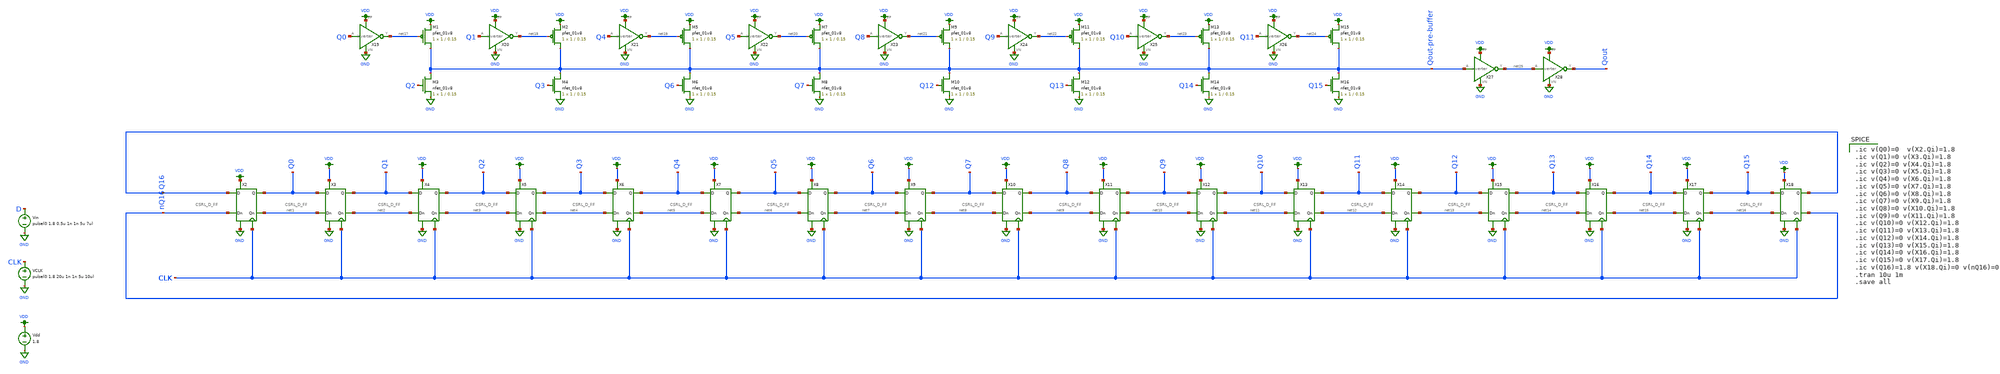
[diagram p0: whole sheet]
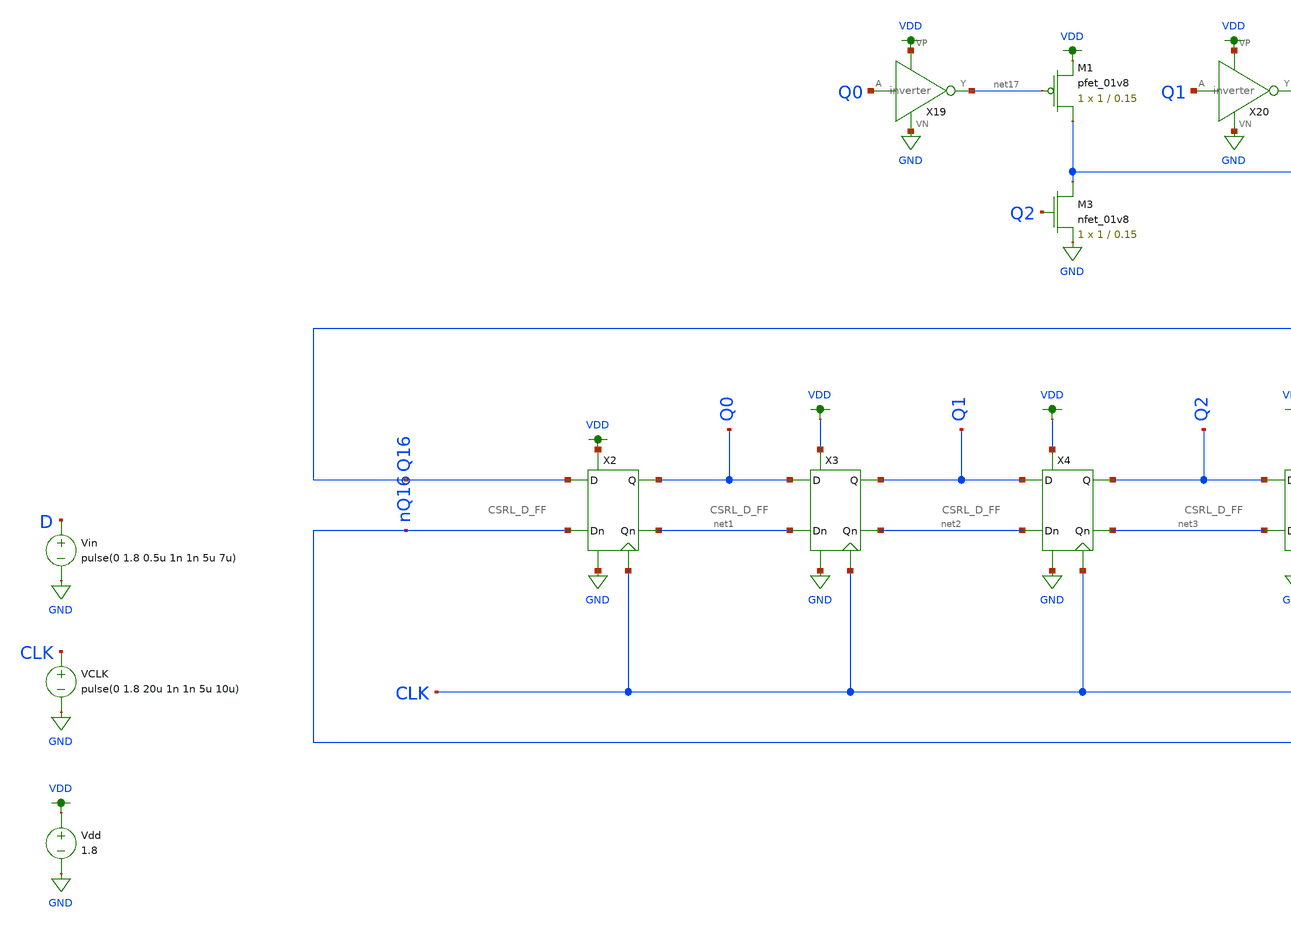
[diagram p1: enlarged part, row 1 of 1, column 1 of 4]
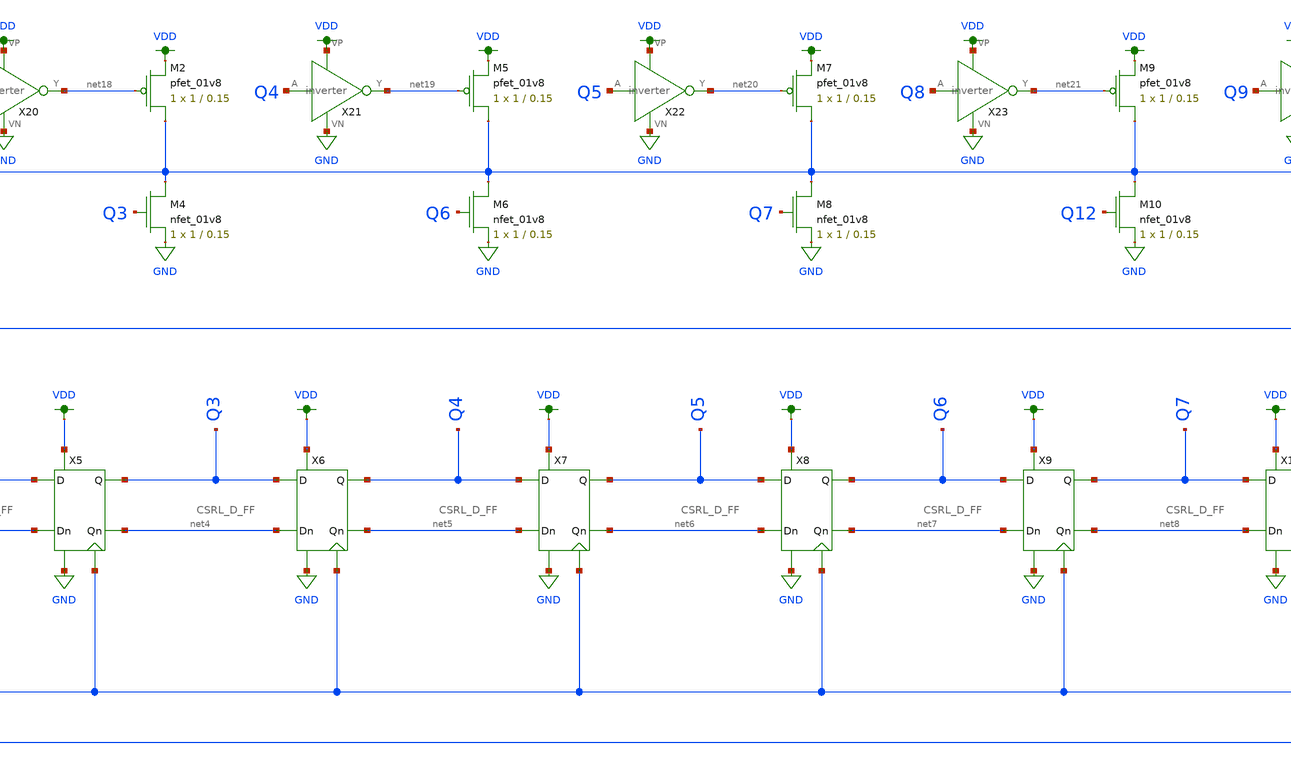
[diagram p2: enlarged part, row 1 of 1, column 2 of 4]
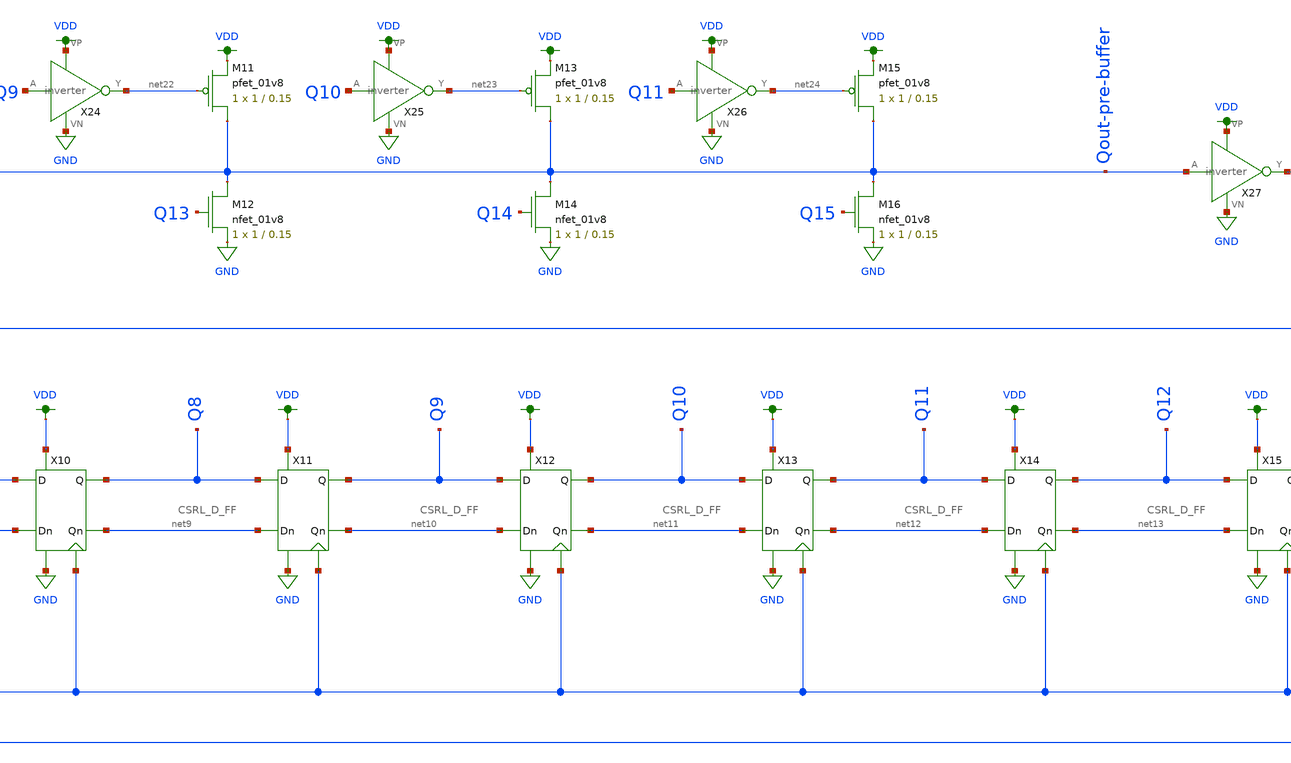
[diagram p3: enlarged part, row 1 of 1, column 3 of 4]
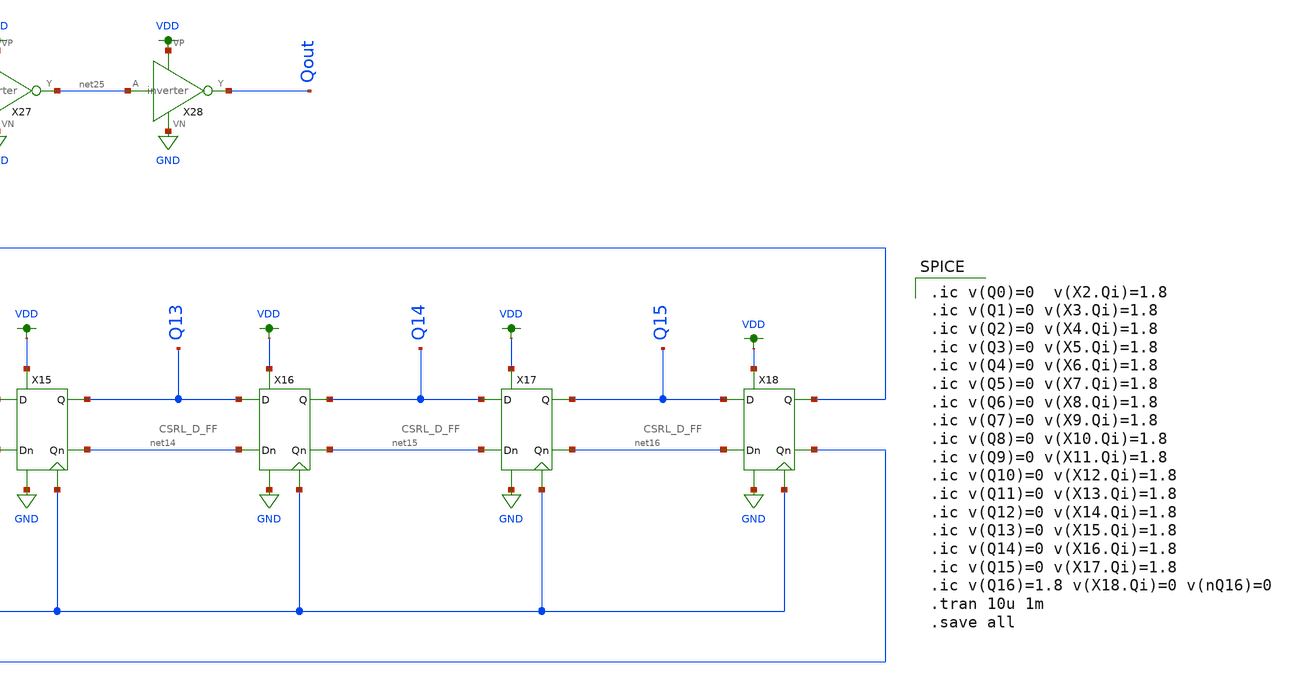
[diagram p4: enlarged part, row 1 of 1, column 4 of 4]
** sch_path: schematic/archive/phi1.sch
**.subckt phi1
Vin D GND pulse(0 1.8 0.5u 1n 1n 5u 7u)
VCLK CLK GND pulse(0 1.8 20u 1n 1n 5u 10u)
Vdd VDD GND 1.8
X2 nQ16 Q16 net1 Q0 GND VDD CLK CSRL_D_FF
X3 net1 Q0 net2 Q1 GND VDD CLK CSRL_D_FF
X4 net2 Q1 net3 Q2 GND VDD CLK CSRL_D_FF
X5 net3 Q2 net4 Q3 GND VDD CLK CSRL_D_FF
X6 net4 Q3 net5 Q4 GND VDD CLK CSRL_D_FF
X7 net5 Q4 net6 Q5 GND VDD CLK CSRL_D_FF
X8 net6 Q5 net7 Q6 GND VDD CLK CSRL_D_FF
X9 net7 Q6 net8 Q7 GND VDD CLK CSRL_D_FF
X10 net8 Q7 net9 Q8 GND VDD CLK CSRL_D_FF
X11 net9 Q8 net10 Q9 GND VDD CLK CSRL_D_FF
X12 net10 Q9 net11 Q10 GND VDD CLK CSRL_D_FF
X13 net11 Q10 net12 Q11 GND VDD CLK CSRL_D_FF
X14 net12 Q11 net13 Q12 GND VDD CLK CSRL_D_FF
X15 net13 Q12 net14 Q13 GND VDD CLK CSRL_D_FF
X16 net14 Q13 net15 Q14 GND VDD CLK CSRL_D_FF
X18 net16 Q15 nQ16 Q16 GND VDD CLK CSRL_D_FF
X17 net15 Q14 net16 Q15 GND VDD CLK CSRL_D_FF
XM1 Qout-pre-buffer net17 VDD VDD sky130_fd_pr__pfet_01v8 L=0.15 W=1 nf=1 ad='int((nf+1)/2) * W/nf * 0.29'
+ as='int((nf+2)/2) * W/nf * 0.29' pd='2*int((nf+1)/2) * (W/nf + 0.29)' ps='2*int((nf+2)/2) * (W/nf + 0.29)'
+ nrd='0.29 / W' nrs='0.29 / W' sa=0 sb=0 sd=0 mult=1 m=1
XM2 Qout-pre-buffer net18 VDD VDD sky130_fd_pr__pfet_01v8 L=0.15 W=1 nf=1 ad='int((nf+1)/2) * W/nf * 0.29'
+ as='int((nf+2)/2) * W/nf * 0.29' pd='2*int((nf+1)/2) * (W/nf + 0.29)' ps='2*int((nf+2)/2) * (W/nf + 0.29)'
+ nrd='0.29 / W' nrs='0.29 / W' sa=0 sb=0 sd=0 mult=1 m=1
X19 Q0 net17 VDD GND inverter
X20 Q1 net18 VDD GND inverter
XM3 Qout-pre-buffer Q2 GND GND sky130_fd_pr__nfet_01v8 L=0.15 W=1 nf=1 ad='int((nf+1)/2) * W/nf * 0.29'
+ as='int((nf+2)/2) * W/nf * 0.29' pd='2*int((nf+1)/2) * (W/nf + 0.29)' ps='2*int((nf+2)/2) * (W/nf + 0.29)'
+ nrd='0.29 / W' nrs='0.29 / W' sa=0 sb=0 sd=0 mult=1 m=1
XM4 Qout-pre-buffer Q3 GND GND sky130_fd_pr__nfet_01v8 L=0.15 W=1 nf=1 ad='int((nf+1)/2) * W/nf * 0.29'
+ as='int((nf+2)/2) * W/nf * 0.29' pd='2*int((nf+1)/2) * (W/nf + 0.29)' ps='2*int((nf+2)/2) * (W/nf + 0.29)'
+ nrd='0.29 / W' nrs='0.29 / W' sa=0 sb=0 sd=0 mult=1 m=1
XM5 Qout-pre-buffer net19 VDD VDD sky130_fd_pr__pfet_01v8 L=0.15 W=1 nf=1 ad='int((nf+1)/2) * W/nf * 0.29'
+ as='int((nf+2)/2) * W/nf * 0.29' pd='2*int((nf+1)/2) * (W/nf + 0.29)' ps='2*int((nf+2)/2) * (W/nf + 0.29)'
+ nrd='0.29 / W' nrs='0.29 / W' sa=0 sb=0 sd=0 mult=1 m=1
X21 Q4 net19 VDD GND inverter
XM6 Qout-pre-buffer Q6 GND GND sky130_fd_pr__nfet_01v8 L=0.15 W=1 nf=1 ad='int((nf+1)/2) * W/nf * 0.29'
+ as='int((nf+2)/2) * W/nf * 0.29' pd='2*int((nf+1)/2) * (W/nf + 0.29)' ps='2*int((nf+2)/2) * (W/nf + 0.29)'
+ nrd='0.29 / W' nrs='0.29 / W' sa=0 sb=0 sd=0 mult=1 m=1
XM7 Qout-pre-buffer net20 VDD VDD sky130_fd_pr__pfet_01v8 L=0.15 W=1 nf=1 ad='int((nf+1)/2) * W/nf * 0.29'
+ as='int((nf+2)/2) * W/nf * 0.29' pd='2*int((nf+1)/2) * (W/nf + 0.29)' ps='2*int((nf+2)/2) * (W/nf + 0.29)'
+ nrd='0.29 / W' nrs='0.29 / W' sa=0 sb=0 sd=0 mult=1 m=1
X22 Q5 net20 VDD GND inverter
XM8 Qout-pre-buffer Q7 GND GND sky130_fd_pr__nfet_01v8 L=0.15 W=1 nf=1 ad='int((nf+1)/2) * W/nf * 0.29'
+ as='int((nf+2)/2) * W/nf * 0.29' pd='2*int((nf+1)/2) * (W/nf + 0.29)' ps='2*int((nf+2)/2) * (W/nf + 0.29)'
+ nrd='0.29 / W' nrs='0.29 / W' sa=0 sb=0 sd=0 mult=1 m=1
XM9 Qout-pre-buffer net21 VDD VDD sky130_fd_pr__pfet_01v8 L=0.15 W=1 nf=1 ad='int((nf+1)/2) * W/nf * 0.29'
+ as='int((nf+2)/2) * W/nf * 0.29' pd='2*int((nf+1)/2) * (W/nf + 0.29)' ps='2*int((nf+2)/2) * (W/nf + 0.29)'
+ nrd='0.29 / W' nrs='0.29 / W' sa=0 sb=0 sd=0 mult=1 m=1
X23 Q8 net21 VDD GND inverter
XM10 Qout-pre-buffer Q12 GND GND sky130_fd_pr__nfet_01v8 L=0.15 W=1 nf=1 ad='int((nf+1)/2) * W/nf * 0.29'
+ as='int((nf+2)/2) * W/nf * 0.29' pd='2*int((nf+1)/2) * (W/nf + 0.29)' ps='2*int((nf+2)/2) * (W/nf + 0.29)'
+ nrd='0.29 / W' nrs='0.29 / W' sa=0 sb=0 sd=0 mult=1 m=1
XM11 Qout-pre-buffer net22 VDD VDD sky130_fd_pr__pfet_01v8 L=0.15 W=1 nf=1 ad='int((nf+1)/2) * W/nf * 0.29'
+ as='int((nf+2)/2) * W/nf * 0.29' pd='2*int((nf+1)/2) * (W/nf + 0.29)' ps='2*int((nf+2)/2) * (W/nf + 0.29)'
+ nrd='0.29 / W' nrs='0.29 / W' sa=0 sb=0 sd=0 mult=1 m=1
X24 Q9 net22 VDD GND inverter
XM12 Qout-pre-buffer Q13 GND GND sky130_fd_pr__nfet_01v8 L=0.15 W=1 nf=1 ad='int((nf+1)/2) * W/nf * 0.29'
+ as='int((nf+2)/2) * W/nf * 0.29' pd='2*int((nf+1)/2) * (W/nf + 0.29)' ps='2*int((nf+2)/2) * (W/nf + 0.29)'
+ nrd='0.29 / W' nrs='0.29 / W' sa=0 sb=0 sd=0 mult=1 m=1
XM13 Qout-pre-buffer net23 VDD VDD sky130_fd_pr__pfet_01v8 L=0.15 W=1 nf=1 ad='int((nf+1)/2) * W/nf * 0.29'
+ as='int((nf+2)/2) * W/nf * 0.29' pd='2*int((nf+1)/2) * (W/nf + 0.29)' ps='2*int((nf+2)/2) * (W/nf + 0.29)'
+ nrd='0.29 / W' nrs='0.29 / W' sa=0 sb=0 sd=0 mult=1 m=1
X25 Q10 net23 VDD GND inverter
XM14 Qout-pre-buffer Q14 GND GND sky130_fd_pr__nfet_01v8 L=0.15 W=1 nf=1 ad='int((nf+1)/2) * W/nf * 0.29'
+ as='int((nf+2)/2) * W/nf * 0.29' pd='2*int((nf+1)/2) * (W/nf + 0.29)' ps='2*int((nf+2)/2) * (W/nf + 0.29)'
+ nrd='0.29 / W' nrs='0.29 / W' sa=0 sb=0 sd=0 mult=1 m=1
XM15 Qout-pre-buffer net24 VDD VDD sky130_fd_pr__pfet_01v8 L=0.15 W=1 nf=1 ad='int((nf+1)/2) * W/nf * 0.29'
+ as='int((nf+2)/2) * W/nf * 0.29' pd='2*int((nf+1)/2) * (W/nf + 0.29)' ps='2*int((nf+2)/2) * (W/nf + 0.29)'
+ nrd='0.29 / W' nrs='0.29 / W' sa=0 sb=0 sd=0 mult=1 m=1
X26 Q11 net24 VDD GND inverter
XM16 Qout-pre-buffer Q15 GND GND sky130_fd_pr__nfet_01v8 L=0.15 W=1 nf=1 ad='int((nf+1)/2) * W/nf * 0.29'
+ as='int((nf+2)/2) * W/nf * 0.29' pd='2*int((nf+1)/2) * (W/nf + 0.29)' ps='2*int((nf+2)/2) * (W/nf + 0.29)'
+ nrd='0.29 / W' nrs='0.29 / W' sa=0 sb=0 sd=0 mult=1 m=1
X27 Qout-pre-buffer net25 VDD GND inverter
X28 net25 Qout VDD GND inverter
**** begin user architecture code

.ic v(Q0)=0  v(X2.Qi)=1.8
.ic v(Q1)=0 v(X3.Qi)=1.8
.ic v(Q2)=0 v(X4.Qi)=1.8
.ic v(Q3)=0 v(X5.Qi)=1.8
.ic v(Q4)=0 v(X6.Qi)=1.8
.ic v(Q5)=0 v(X7.Qi)=1.8
.ic v(Q6)=0 v(X8.Qi)=1.8
.ic v(Q7)=0 v(X9.Qi)=1.8
.ic v(Q8)=0 v(X10.Qi)=1.8
.ic v(Q9)=0 v(X11.Qi)=1.8
.ic v(Q10)=0 v(X12.Qi)=1.8
.ic v(Q11)=0 v(X13.Qi)=1.8
.ic v(Q12)=0 v(X14.Qi)=1.8
.ic v(Q13)=0 v(X15.Qi)=1.8
.ic v(Q14)=0 v(X16.Qi)=1.8
.ic v(Q15)=0 v(X17.Qi)=1.8
.ic v(Q16)=1.8 v(X18.Qi)=0 v(nQ16)=0
.tran 10u 1m
.save all


.option wnflag=1
.param MC_SWITCH=0.0
.lib /media/qdeng/526448C32060CF5C/skywater/skywater-pdk/libraries/sky130_fd_pr_ngspice/latest/models/sky130.lib.spice tt

**** end user architecture code
**.ends

* expanding   symbol:  /home/madvlsi/Documents/MADVLSI-Final_Project/schematic/CSRL_D_FF.sym # of
*+ pins=7
** sym_path: schematic/CSRL_D_FF.sym
** sch_path: schematic/CSRL_D_FF.sch
.subckt CSRL_D_FF Dn D Qn Q VN VP CLK
*.ipin Dn
*.ipin D
*.iopin VP
*.iopin VN
*.iopin CLK
*.opin Qn
*.opin Q
XM1 net5 CLK VP VDD sky130_fd_pr__pfet_01v8 L=0.15 W=1 nf=1 ad='int((nf+1)/2) * W/nf * 0.29' as='int((nf+2)/2) * W/nf * 0.29'
+ pd='2*int((nf+1)/2) * (W/nf + 0.29)' ps='2*int((nf+2)/2) * (W/nf + 0.29)' nrd='0.29 / W' nrs='0.29 / W'
+ sa=0 sb=0 sd=0 mult=1 m=1
XM2 net6 CLK VP VDD sky130_fd_pr__pfet_01v8 L=0.15 W=1 nf=1 ad='int((nf+1)/2) * W/nf * 0.29' as='int((nf+2)/2) * W/nf * 0.29'
+ pd='2*int((nf+1)/2) * (W/nf + 0.29)' ps='2*int((nf+2)/2) * (W/nf + 0.29)' nrd='0.29 / W' nrs='0.29 / W'
+ sa=0 sb=0 sd=0 mult=1 m=1
XM3 net3 CLK Q GND sky130_fd_pr__nfet_01v8 L=0.15 W=1 nf=1 ad='int((nf+1)/2) * W/nf * 0.29' as='int((nf+2)/2) * W/nf * 0.29'
+ pd='2*int((nf+1)/2) * (W/nf + 0.29)' ps='2*int((nf+2)/2) * (W/nf + 0.29)' nrd='0.29 / W' nrs='0.29 / W'
+ sa=0 sb=0 sd=0 mult=1 m=1
XM4 net4 CLK Qn GND sky130_fd_pr__nfet_01v8 L=0.15 W=1 nf=1 ad='int((nf+1)/2) * W/nf * 0.29' as='int((nf+2)/2) * W/nf * 0.29'
+ pd='2*int((nf+1)/2) * (W/nf + 0.29)' ps='2*int((nf+2)/2) * (W/nf + 0.29)' nrd='0.29 / W' nrs='0.29 / W'
+ sa=0 sb=0 sd=0 mult=1 m=1
XM5 Q Qn net6 VDD sky130_fd_pr__pfet_01v8 L=0.15 W=1 nf=1 ad='int((nf+1)/2) * W/nf * 0.29' as='int((nf+2)/2) * W/nf * 0.29'
+ pd='2*int((nf+1)/2) * (W/nf + 0.29)' ps='2*int((nf+2)/2) * (W/nf + 0.29)' nrd='0.29 / W' nrs='0.29 / W'
+ sa=0 sb=0 sd=0 mult=1 m=1
XM6 VN Qn Q GND sky130_fd_pr__nfet_01v8 L=0.15 W=1 nf=1 ad='int((nf+1)/2) * W/nf * 0.29' as='int((nf+2)/2) * W/nf * 0.29'
+ pd='2*int((nf+1)/2) * (W/nf + 0.29)' ps='2*int((nf+2)/2) * (W/nf + 0.29)' nrd='0.29 / W' nrs='0.29 / W'
+ sa=0 sb=0 sd=0 mult=1 m=1
XM7 Qn Q net5 VDD sky130_fd_pr__pfet_01v8 L=0.15 W=1 nf=1 ad='int((nf+1)/2) * W/nf * 0.29' as='int((nf+2)/2) * W/nf * 0.29'
+ pd='2*int((nf+1)/2) * (W/nf + 0.29)' ps='2*int((nf+2)/2) * (W/nf + 0.29)' nrd='0.29 / W' nrs='0.29 / W'
+ sa=0 sb=0 sd=0 mult=1 m=1
XM8 VN Q Qn GND sky130_fd_pr__nfet_01v8 L=0.15 W=1 nf=1 ad='int((nf+1)/2) * W/nf * 0.29' as='int((nf+2)/2) * W/nf * 0.29'
+ pd='2*int((nf+1)/2) * (W/nf + 0.29)' ps='2*int((nf+2)/2) * (W/nf + 0.29)' nrd='0.29 / W' nrs='0.29 / W'
+ sa=0 sb=0 sd=0 mult=1 m=1
XM9 net4 CLK Dn VDD sky130_fd_pr__pfet_01v8 L=0.15 W=1 nf=1 ad='int((nf+1)/2) * W/nf * 0.29' as='int((nf+2)/2) * W/nf * 0.29'
+ pd='2*int((nf+1)/2) * (W/nf + 0.29)' ps='2*int((nf+2)/2) * (W/nf + 0.29)' nrd='0.29 / W' nrs='0.29 / W'
+ sa=0 sb=0 sd=0 mult=1 m=1
XM10 net3 CLK D VDD sky130_fd_pr__pfet_01v8 L=0.15 W=1 nf=1 ad='int((nf+1)/2) * W/nf * 0.29' as='int((nf+2)/2) * W/nf * 0.29'
+ pd='2*int((nf+1)/2) * (W/nf + 0.29)' ps='2*int((nf+2)/2) * (W/nf + 0.29)' nrd='0.29 / W' nrs='0.29 / W'
+ sa=0 sb=0 sd=0 mult=1 m=1
XM11 VN CLK net1 GND sky130_fd_pr__nfet_01v8 L=0.15 W=1 nf=1 ad='int((nf+1)/2) * W/nf * 0.29' as='int((nf+2)/2) * W/nf * 0.29'
+ pd='2*int((nf+1)/2) * (W/nf + 0.29)' ps='2*int((nf+2)/2) * (W/nf + 0.29)' nrd='0.29 / W' nrs='0.29 / W'
+ sa=0 sb=0 sd=0 mult=1 m=1
XM12 VN CLK net2 GND sky130_fd_pr__nfet_01v8 L=0.15 W=1 nf=1 ad='int((nf+1)/2) * W/nf * 0.29' as='int((nf+2)/2) * W/nf * 0.29'
+ pd='2*int((nf+1)/2) * (W/nf + 0.29)' ps='2*int((nf+2)/2) * (W/nf + 0.29)' nrd='0.29 / W' nrs='0.29 / W'
+ sa=0 sb=0 sd=0 mult=1 m=1
XM13 VP net3 net4 VDD sky130_fd_pr__pfet_01v8 L=0.15 W=1 nf=1 ad='int((nf+1)/2) * W/nf * 0.29' as='int((nf+2)/2) * W/nf * 0.29'
+ pd='2*int((nf+1)/2) * (W/nf + 0.29)' ps='2*int((nf+2)/2) * (W/nf + 0.29)' nrd='0.29 / W' nrs='0.29 / W'
+ sa=0 sb=0 sd=0 mult=1 m=1
XM14 VP net4 net3 VDD sky130_fd_pr__pfet_01v8 L=0.15 W=1 nf=1 ad='int((nf+1)/2) * W/nf * 0.29' as='int((nf+2)/2) * W/nf * 0.29'
+ pd='2*int((nf+1)/2) * (W/nf + 0.29)' ps='2*int((nf+2)/2) * (W/nf + 0.29)' nrd='0.29 / W' nrs='0.29 / W'
+ sa=0 sb=0 sd=0 mult=1 m=1
XM15 net3 net4 net1 GND sky130_fd_pr__nfet_01v8 L=0.15 W=1 nf=1 ad='int((nf+1)/2) * W/nf * 0.29' as='int((nf+2)/2) * W/nf * 0.29'
+ pd='2*int((nf+1)/2) * (W/nf + 0.29)' ps='2*int((nf+2)/2) * (W/nf + 0.29)' nrd='0.29 / W' nrs='0.29 / W'
+ sa=0 sb=0 sd=0 mult=1 m=1
XM16 net4 net3 net2 GND sky130_fd_pr__nfet_01v8 L=0.15 W=1 nf=1 ad='int((nf+1)/2) * W/nf * 0.29' as='int((nf+2)/2) * W/nf * 0.29'
+ pd='2*int((nf+1)/2) * (W/nf + 0.29)' ps='2*int((nf+2)/2) * (W/nf + 0.29)' nrd='0.29 / W' nrs='0.29 / W'
+ sa=0 sb=0 sd=0 mult=1 m=1
XM17 VN CLK net2 GND sky130_fd_pr__nfet_01v8 L=0.15 W=1 nf=1 ad='int((nf+1)/2) * W/nf * 0.29' as='int((nf+2)/2) * W/nf * 0.29'
+ pd='2*int((nf+1)/2) * (W/nf + 0.29)' ps='2*int((nf+2)/2) * (W/nf + 0.29)' nrd='0.29 / W' nrs='0.29 / W'
+ sa=0 sb=0 sd=0 mult=1 m=1
XM18 VN CLK net1 GND sky130_fd_pr__nfet_01v8 L=0.15 W=1 nf=1 ad='int((nf+1)/2) * W/nf * 0.29' as='int((nf+2)/2) * W/nf * 0.29'
+ pd='2*int((nf+1)/2) * (W/nf + 0.29)' ps='2*int((nf+2)/2) * (W/nf + 0.29)' nrd='0.29 / W' nrs='0.29 / W'
+ sa=0 sb=0 sd=0 mult=1 m=1
.ends


* expanding   symbol:  /home/madvlsi/Documents/MADVLSI-Final_Project/schematic/inverter.sym # of
*+ pins=4
** sym_path: schematic/inverter.sym
** sch_path: schematic/inverter.sch
.subckt inverter A Y VP VN
*.opin Y
*.ipin A
*.iopin VP
*.iopin VN
XM3 Y A VP VDD sky130_fd_pr__pfet_01v8 L={Lp} W={Wp} nf=1 ad='int((nf+1)/2) * W/nf * 0.29' as='int((nf+2)/2) * W/nf * 0.29'
+ pd='2*int((nf+1)/2) * (W/nf + 0.29)' ps='2*int((nf+2)/2) * (W/nf + 0.29)' nrd='0.29 / W' nrs='0.29 / W'
+ sa=0 sb=0 sd=0 mult=1 m=1
XM4 Y A VP VDD sky130_fd_pr__pfet_01v8 L={Lp} W={Wp} nf=1 ad='int((nf+1)/2) * W/nf * 0.29' as='int((nf+2)/2) * W/nf * 0.29'
+ pd='2*int((nf+1)/2) * (W/nf + 0.29)' ps='2*int((nf+2)/2) * (W/nf + 0.29)' nrd='0.29 / W' nrs='0.29 / W'
+ sa=0 sb=0 sd=0 mult=1 m=1
XM5 Y A VN GND sky130_fd_pr__nfet_01v8 L={Lp} W={Wp} nf=1 ad='int((nf+1)/2) * W/nf * 0.29' as='int((nf+2)/2) * W/nf * 0.29'
+ pd='2*int((nf+1)/2) * (W/nf + 0.29)' ps='2*int((nf+2)/2) * (W/nf + 0.29)' nrd='0.29 / W' nrs='0.29 / W'
+ sa=0 sb=0 sd=0 mult=1 m=1
.ends

.GLOBAL GND
.GLOBAL VDD
.end
